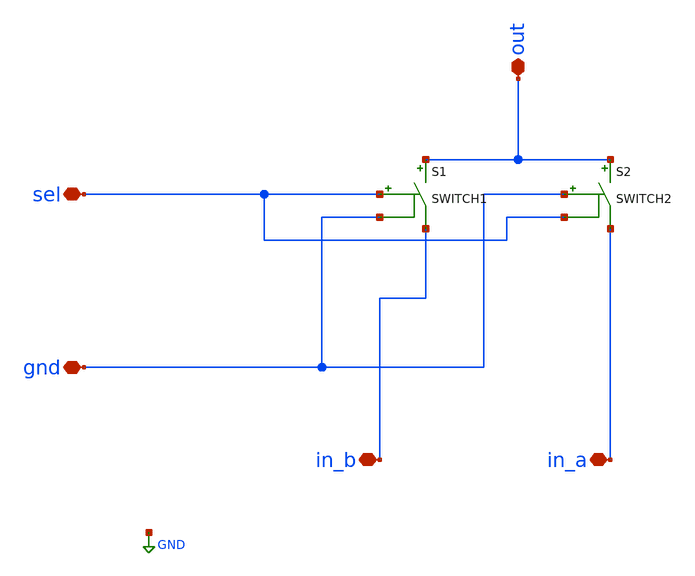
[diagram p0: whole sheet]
** sch_path: design/myopamp/myswitch.sch
**.subckt myswitch gnd sel out in_a in_b
*.iopin gnd
*.iopin sel
*.iopin out
*.iopin in_a
*.iopin in_b
S1 out in_b sel gnd SWITCH1
S2 out in_a gnd sel SWITCH2
**.ends
.GLOBAL GND
.end
